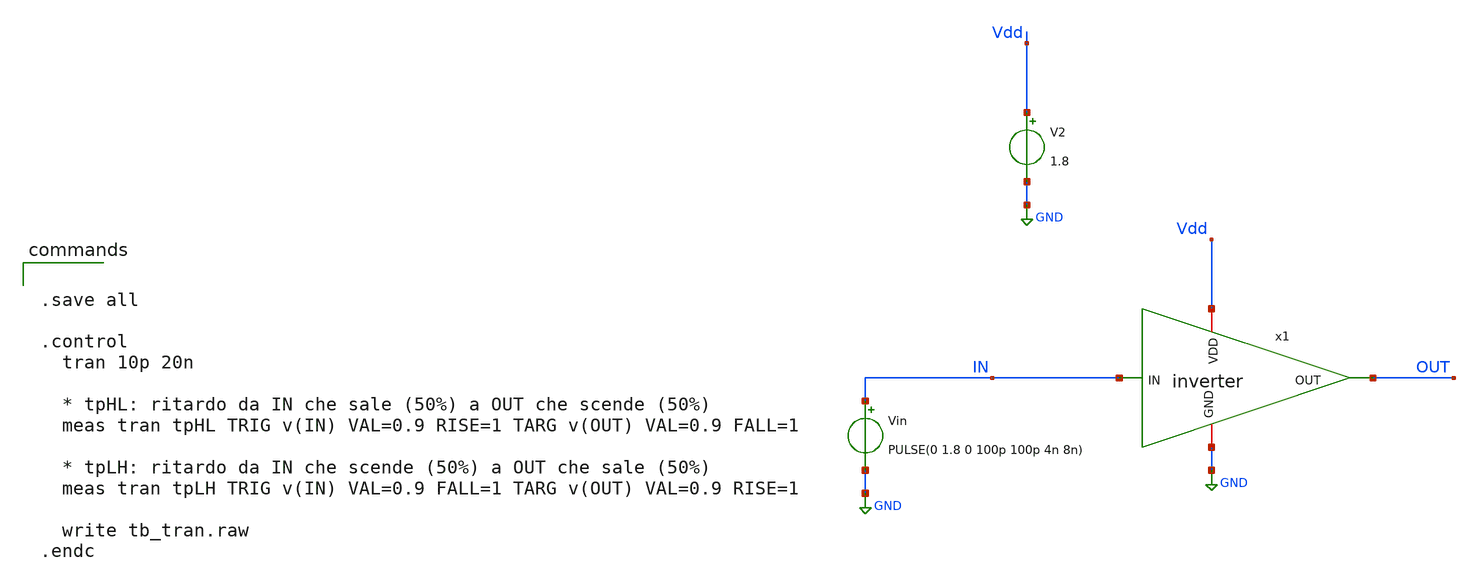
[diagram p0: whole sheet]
** sch_path: 01_xschem_ngspice/soluzioni/lab01/xschem/tb_tran.sch
**.subckt tb_tran
x1 Vdd IN OUT GND inverter
Vin IN GND PULSE(0 1.8 0 100p 100p 4n 8n)
V2 Vdd GND 1.8
**** begin user architecture code

** opencircuitdesign pdks install
.lib $::SKYWATER_MODELS/sky130.lib.spice tt



.save all

.control
  tran 10p 20n

  * tpHL: ritardo da IN che sale (50%) a OUT che scende (50%)
  meas tran tpHL TRIG v(IN) VAL=0.9 RISE=1 TARG v(OUT) VAL=0.9 FALL=1

  * tpLH: ritardo da IN che scende (50%) a OUT che sale (50%)
  meas tran tpLH TRIG v(IN) VAL=0.9 FALL=1 TARG v(OUT) VAL=0.9 RISE=1

  write tb_tran.raw
.endc


**** end user architecture code
**.ends

* expanding   symbol:  inverter.sym # of pins=4
** sym_path: 01_xschem_ngspice/soluzioni/lab01/xschem/inverter.sym
** sch_path: 01_xschem_ngspice/soluzioni/lab01/xschem/inverter.sch
.subckt inverter VDD IN OUT GND
*.ipin IN
*.opin OUT
*.iopin VDD
*.iopin GND
XM1 OUT IN GND GND sky130_fd_pr__nfet_01v8 L=0.15 W=1 nf=1 ad='int((1 + 1)/2) * 1 / 1 * 0.29' as='int((1 + 2)/2) * 1 / 1 * 0.29'
+ pd='2*int((1 + 1)/2) * (1 / 1 + 0.29)' ps='2*int((1 + 2)/2) * (1 / 1 + 0.29)' nrd='0.29 / 1 ' nrs='0.29 / 1 '
+ sa=0 sb=0 sd=0 mult=1 m=1
XM2 OUT IN VDD VDD sky130_fd_pr__pfet_01v8 L=0.15 W=2 nf=1 ad='int((1 + 1)/2) * 2 / 1 * 0.29' as='int((1 + 2)/2) * 2 / 1 * 0.29'
+ pd='2*int((1 + 1)/2) * (2 / 1 + 0.29)' ps='2*int((1 + 2)/2) * (2 / 1 + 0.29)' nrd='0.29 / 2 ' nrs='0.29 / 2 '
+ sa=0 sb=0 sd=0 mult=1 m=1
.ends

.GLOBAL GND
.end
